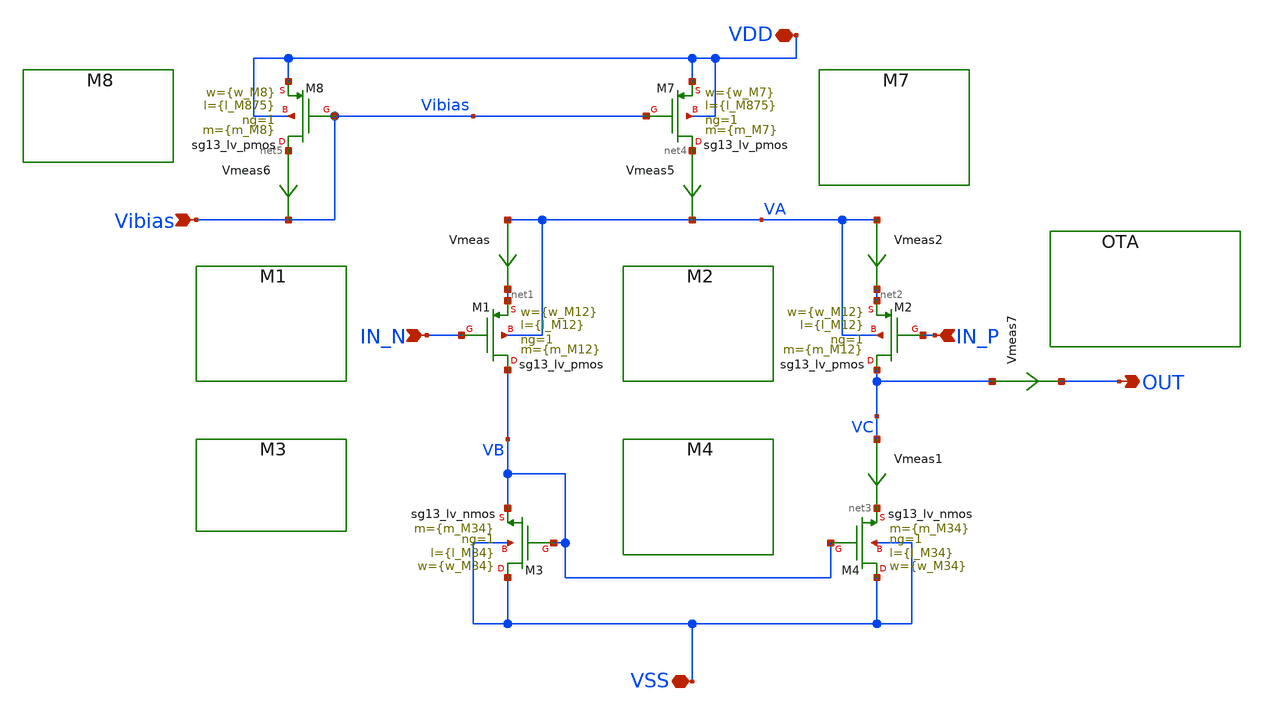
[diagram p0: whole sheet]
** sch_path: xschem/Tareas/Tarea_2/OTA1.sch
**.subckt OTA1 IN_N IN_P Vibias OUT VDD VSS
*.ipin IN_N
*.ipin IN_P
*.ipin Vibias
*.opin OUT
*.iopin VDD
*.iopin VSS
XM1 VB IN_N net1 VA sg13_lv_pmos w={w_M12} l={l_M12} ng=1 m={m_M12} mm_ok=1
XM3 VSS VB VB VSS sg13_lv_nmos w={w_M34} l={l_M34} ng=1 m={m_M34} mm_ok=1
XM2 VC IN_P net2 VA sg13_lv_pmos w={w_M12} l={l_M12} ng=1 m={m_M12} mm_ok=1
XM4 VSS VB net3 VSS sg13_lv_nmos w={w_M34} l={l_M34} ng=1 m={m_M34} mm_ok=1
XM7 net4 Vibias VDD VDD sg13_lv_pmos w={w_M7} l={l_M875} ng=1 m={m_M7} mm_ok=1
XM8 net5 Vibias VDD VDD sg13_lv_pmos w={w_M8} l={l_M875} ng=1 m={m_M8} mm_ok=1
Vmeas VA net1 0
.save i(vmeas)
Vmeas1 VC net3 0
.save i(vmeas1)
Vmeas2 VA net2 0
.save i(vmeas2)
Vmeas5 net4 VA 0
.save i(vmeas5)
Vmeas6 net5 Vibias 0
.save i(vmeas6)
Vmeas7 VC OUT 0
.save i(vmeas7)
**.ends
.end
